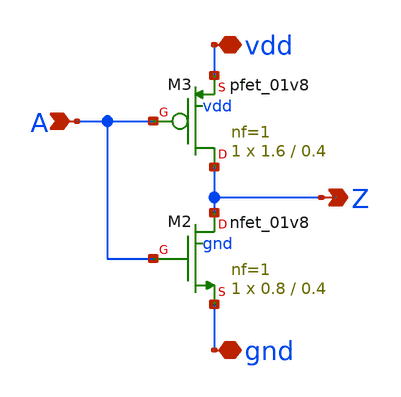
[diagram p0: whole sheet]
** sch_path: sram_2_16_scn4m/pinv_11.sch
**.subckt pinv_11 A Z vdd gnd
*.ipin A
*.opin Z
*.iopin vdd
*.iopin gnd
XM2 Z A gnd gnd sky130_fd_pr__nfet_01v8 L=0.4 W=0.8 nf=1 ad='int((nf+1)/2) * W/nf * 0.29' as='int((nf+2)/2) * W/nf * 0.29'
+ pd='2*int((nf+1)/2) * (W/nf + 0.29)' ps='2*int((nf+2)/2) * (W/nf + 0.29)' nrd='0.29 / W' nrs='0.29 / W'
+ sa=0 sb=0 sd=0 mult=1 m=1
XM3 Z A vdd vdd sky130_fd_pr__pfet_01v8 L=0.4 W=1.6 nf=1 ad='int((nf+1)/2) * W/nf * 0.29' as='int((nf+2)/2) * W/nf * 0.29'
+ pd='2*int((nf+1)/2) * (W/nf + 0.29)' ps='2*int((nf+2)/2) * (W/nf + 0.29)' nrd='0.29 / W' nrs='0.29 / W'
+ sa=0 sb=0 sd=0 mult=1 m=1
**.ends
.end
